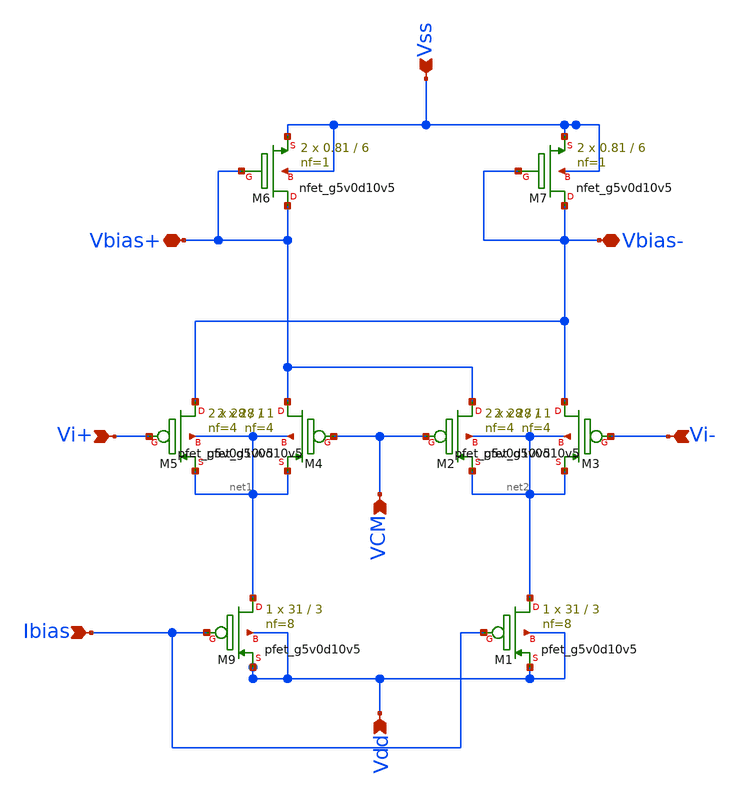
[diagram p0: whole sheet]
** sch_path: xschem/CMFB.sch
**.subckt CMFB VCM Vss Vdd Vi+ Vi- Ibias Vbias+ Vbias-
*.ipin VCM
*.ipin Vss
*.ipin Vdd
*.ipin Vi+
*.ipin Vi-
*.ipin Ibias
*.iopin Vbias+
*.iopin Vbias-
XM9 net1 Ibias Vdd Vdd sky130_fd_pr__pfet_g5v0d10v5 L=3 W=31 nf=8 ad='int((8 + 1)/2) * 31 / 8 * 0.29'
+ as='int((8 + 2)/2) * 31 / 8 * 0.29' pd='2*int((8 + 1)/2) * (31 / 8 + 0.29)' ps='2*int((8 + 2)/2) * (31 / 8 + 0.29)'
+ nrd='0.29 / 31 ' nrs='0.29 / 31 ' sa=0 sb=0 sd=0 mult=1 m=1
XM1 net2 Ibias Vdd Vdd sky130_fd_pr__pfet_g5v0d10v5 L=3 W=31 nf=8 ad='int((8 + 1)/2) * 31 / 8 * 0.29'
+ as='int((8 + 2)/2) * 31 / 8 * 0.29' pd='2*int((8 + 1)/2) * (31 / 8 + 0.29)' ps='2*int((8 + 2)/2) * (31 / 8 + 0.29)'
+ nrd='0.29 / 31 ' nrs='0.29 / 31 ' sa=0 sb=0 sd=0 mult=1 m=1
XM5 Vbias- Vi+ net1 net1 sky130_fd_pr__pfet_g5v0d10v5 L=1 W=28 nf=4 ad='int((4 + 1)/2) * 28 / 4 * 0.29'
+ as='int((4 + 2)/2) * 28 / 4 * 0.29' pd='2*int((4 + 1)/2) * (28 / 4 + 0.29)' ps='2*int((4 + 2)/2) * (28 / 4 + 0.29)'
+ nrd='0.29 / 28 ' nrs='0.29 / 28 ' sa=0 sb=0 sd=0 mult=2 m=2
XM2 Vbias+ VCM net2 net2 sky130_fd_pr__pfet_g5v0d10v5 L=1 W=28 nf=4 ad='int((4 + 1)/2) * 28 / 4 * 0.29'
+ as='int((4 + 2)/2) * 28 / 4 * 0.29' pd='2*int((4 + 1)/2) * (28 / 4 + 0.29)' ps='2*int((4 + 2)/2) * (28 / 4 + 0.29)'
+ nrd='0.29 / 28 ' nrs='0.29 / 28 ' sa=0 sb=0 sd=0 mult=2 m=2
XM4 Vbias+ VCM net1 net1 sky130_fd_pr__pfet_g5v0d10v5 L=1 W=28 nf=4 ad='int((4 + 1)/2) * 28 / 4 * 0.29'
+ as='int((4 + 2)/2) * 28 / 4 * 0.29' pd='2*int((4 + 1)/2) * (28 / 4 + 0.29)' ps='2*int((4 + 2)/2) * (28 / 4 + 0.29)'
+ nrd='0.29 / 28 ' nrs='0.29 / 28 ' sa=0 sb=0 sd=0 mult=2 m=2
XM3 Vbias- Vi- net2 net2 sky130_fd_pr__pfet_g5v0d10v5 L=1 W=28 nf=4 ad='int((4 + 1)/2) * 28 / 4 * 0.29'
+ as='int((4 + 2)/2) * 28 / 4 * 0.29' pd='2*int((4 + 1)/2) * (28 / 4 + 0.29)' ps='2*int((4 + 2)/2) * (28 / 4 + 0.29)'
+ nrd='0.29 / 28 ' nrs='0.29 / 28 ' sa=0 sb=0 sd=0 mult=2 m=2
XM6 Vbias+ Vbias+ Vss Vss sky130_fd_pr__nfet_g5v0d10v5 L=6 W=0.81 nf=1 ad='int((1 + 1)/2) * 0.81 / 1 * 0.29'
+ as='int((1 + 2)/2) * 0.81 / 1 * 0.29' pd='2*int((1 + 1)/2) * (0.81 / 1 + 0.29)' ps='2*int((1 + 2)/2) * (0.81 / 1 + 0.29)'
+ nrd='0.29 / 0.81 ' nrs='0.29 / 0.81 ' sa=0 sb=0 sd=0 mult=2 m=2
XM7 Vbias- Vbias- Vss Vss sky130_fd_pr__nfet_g5v0d10v5 L=6 W=0.81 nf=1 ad='int((1 + 1)/2) * 0.81 / 1 * 0.29'
+ as='int((1 + 2)/2) * 0.81 / 1 * 0.29' pd='2*int((1 + 1)/2) * (0.81 / 1 + 0.29)' ps='2*int((1 + 2)/2) * (0.81 / 1 + 0.29)'
+ nrd='0.29 / 0.81 ' nrs='0.29 / 0.81 ' sa=0 sb=0 sd=0 mult=2 m=2
**.ends
.end
